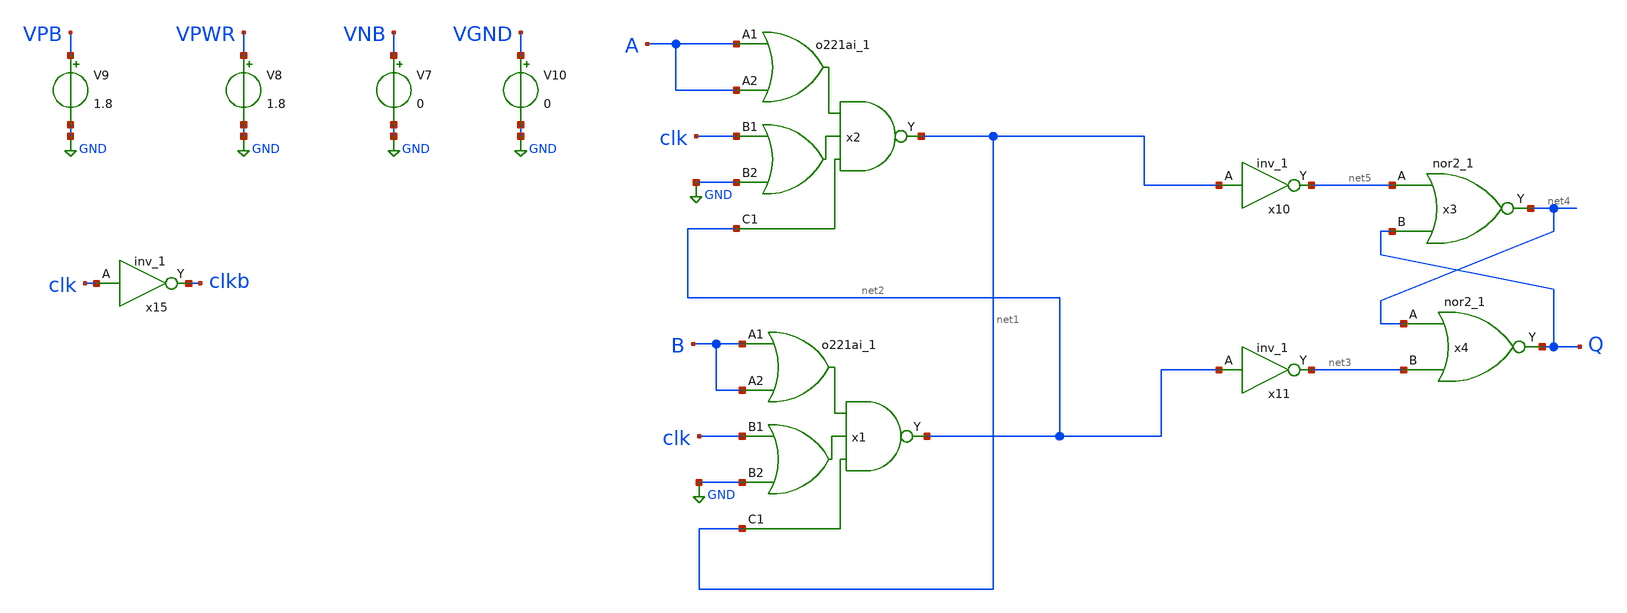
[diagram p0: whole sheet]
** sch_path: cmp/Schematics/cmpoaisch_2.sch
**.subckt cmpoaisch_2
V7 VNB GND 0
V8 VPWR GND 1.8
V9 VPB GND 1.8
V10 VGND GND 0
x15 clk VGND VNB VPB VPWR clkb sky130_fd_sc_hd__inv_1
x10 net1 VGND VNB VPB VPWR net5 sky130_fd_sc_hd__inv_1
x11 net2 VGND VNB VPB VPWR net3 sky130_fd_sc_hd__inv_1
x3 net5 Q VGND VNB VPB VPWR net4 sky130_fd_sc_hd__nor2_1
x4 net4 net3 VGND VNB VPB VPWR Q sky130_fd_sc_hd__nor2_1
x2 A A clk GND net2 VGND VNB VPB VPWR net1 sky130_fd_sc_hd__o221ai_1
x1 B B clk GND net1 VGND VNB VPB VPWR net2 sky130_fd_sc_hd__o221ai_1
**.ends
.GLOBAL GND
.end
